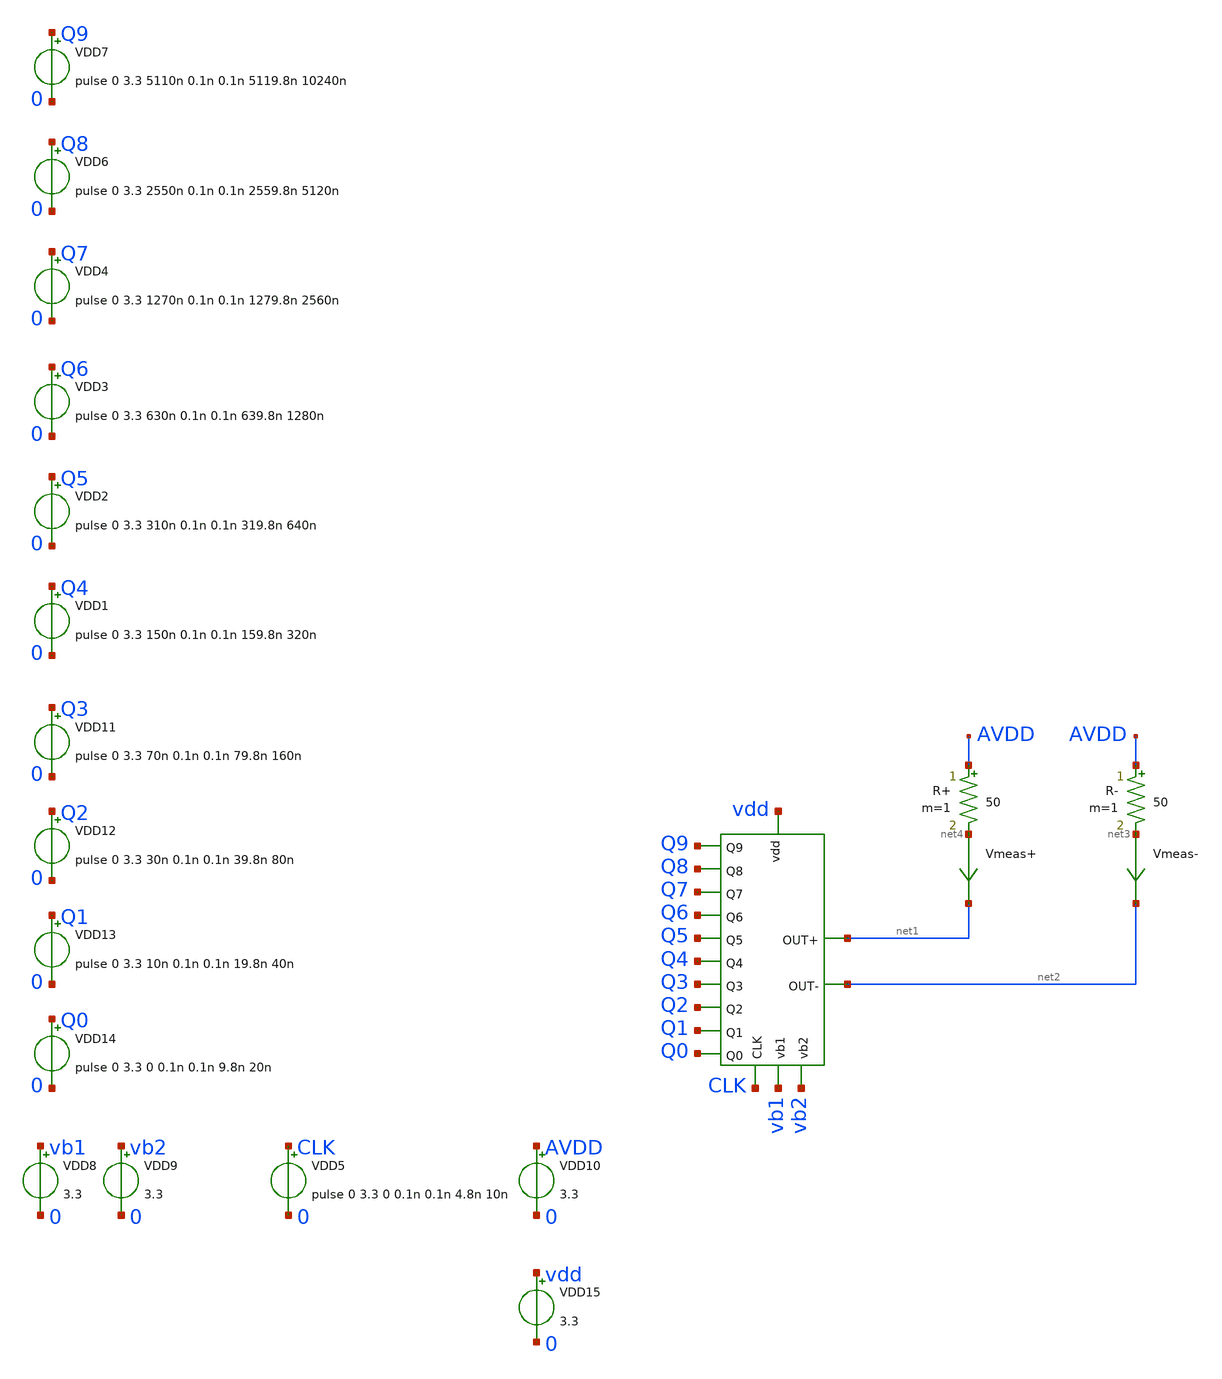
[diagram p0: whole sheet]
** sch_path: initial_notebooks_2023/Current-Steering DAC/DAC/Test_DAC.sch
**.subckt Test_DAC
x1 net2 net1 Q9 Q8 Q7 Q6 Q5 Q4 Q3 Q2 Q1 Q0 CLK vb1 vb2 vdd DAC
VDD1 Q4 0 pulse 0 3.3 150n 0.1n 0.1n 159.8n 320n
VDD2 Q5 0 pulse 0 3.3 310n 0.1n 0.1n 319.8n 640n
VDD3 Q6 0 pulse 0 3.3 630n 0.1n 0.1n 639.8n 1280n
VDD4 Q7 0 pulse 0 3.3 1270n 0.1n 0.1n 1279.8n 2560n
VDD6 Q8 0 pulse 0 3.3 2550n 0.1n 0.1n 2559.8n 5120n
VDD7 Q9 0 pulse 0 3.3 5110n 0.1n 0.1n 5119.8n 10240n
VDD11 Q3 0 pulse 0 3.3 70n 0.1n 0.1n 79.8n 160n
VDD12 Q2 0 pulse 0 3.3 30n 0.1n 0.1n 39.8n 80n
VDD13 Q1 0 pulse 0 3.3 10n 0.1n 0.1n 19.8n 40n
VDD14 Q0 0 pulse 0 3.3 0 0.1n 0.1n 9.8n 20n
VDD5 CLK 0 pulse 0 3.3 0 0.1n 0.1n 4.8n 10n
VDD8 vb1 0 3.3
VDD9 vb2 0 3.3
VDD10 AVDD 0 3.3
VDD15 vdd 0 3.3
R- AVDD net3 50 m=1
R+ AVDD net4 50 m=1
Vmeas+ net4 net1 0
.save i(vmeas+)
Vmeas- net3 net2 0
.save i(vmeas-)
**** begin user architecture code




.include /foss/pdks/gf180mcuC/libs.tech/ngspice/design.ngspice
.lib /foss/pdks/gf180mcuC/libs.tech/ngspice/sm141064.ngspice typical


.control
	tran 1n 1000n
	plot i(Vmeas+)
	write topview.raw
.endc
.save all




**** end user architecture code
**.ends
.end
